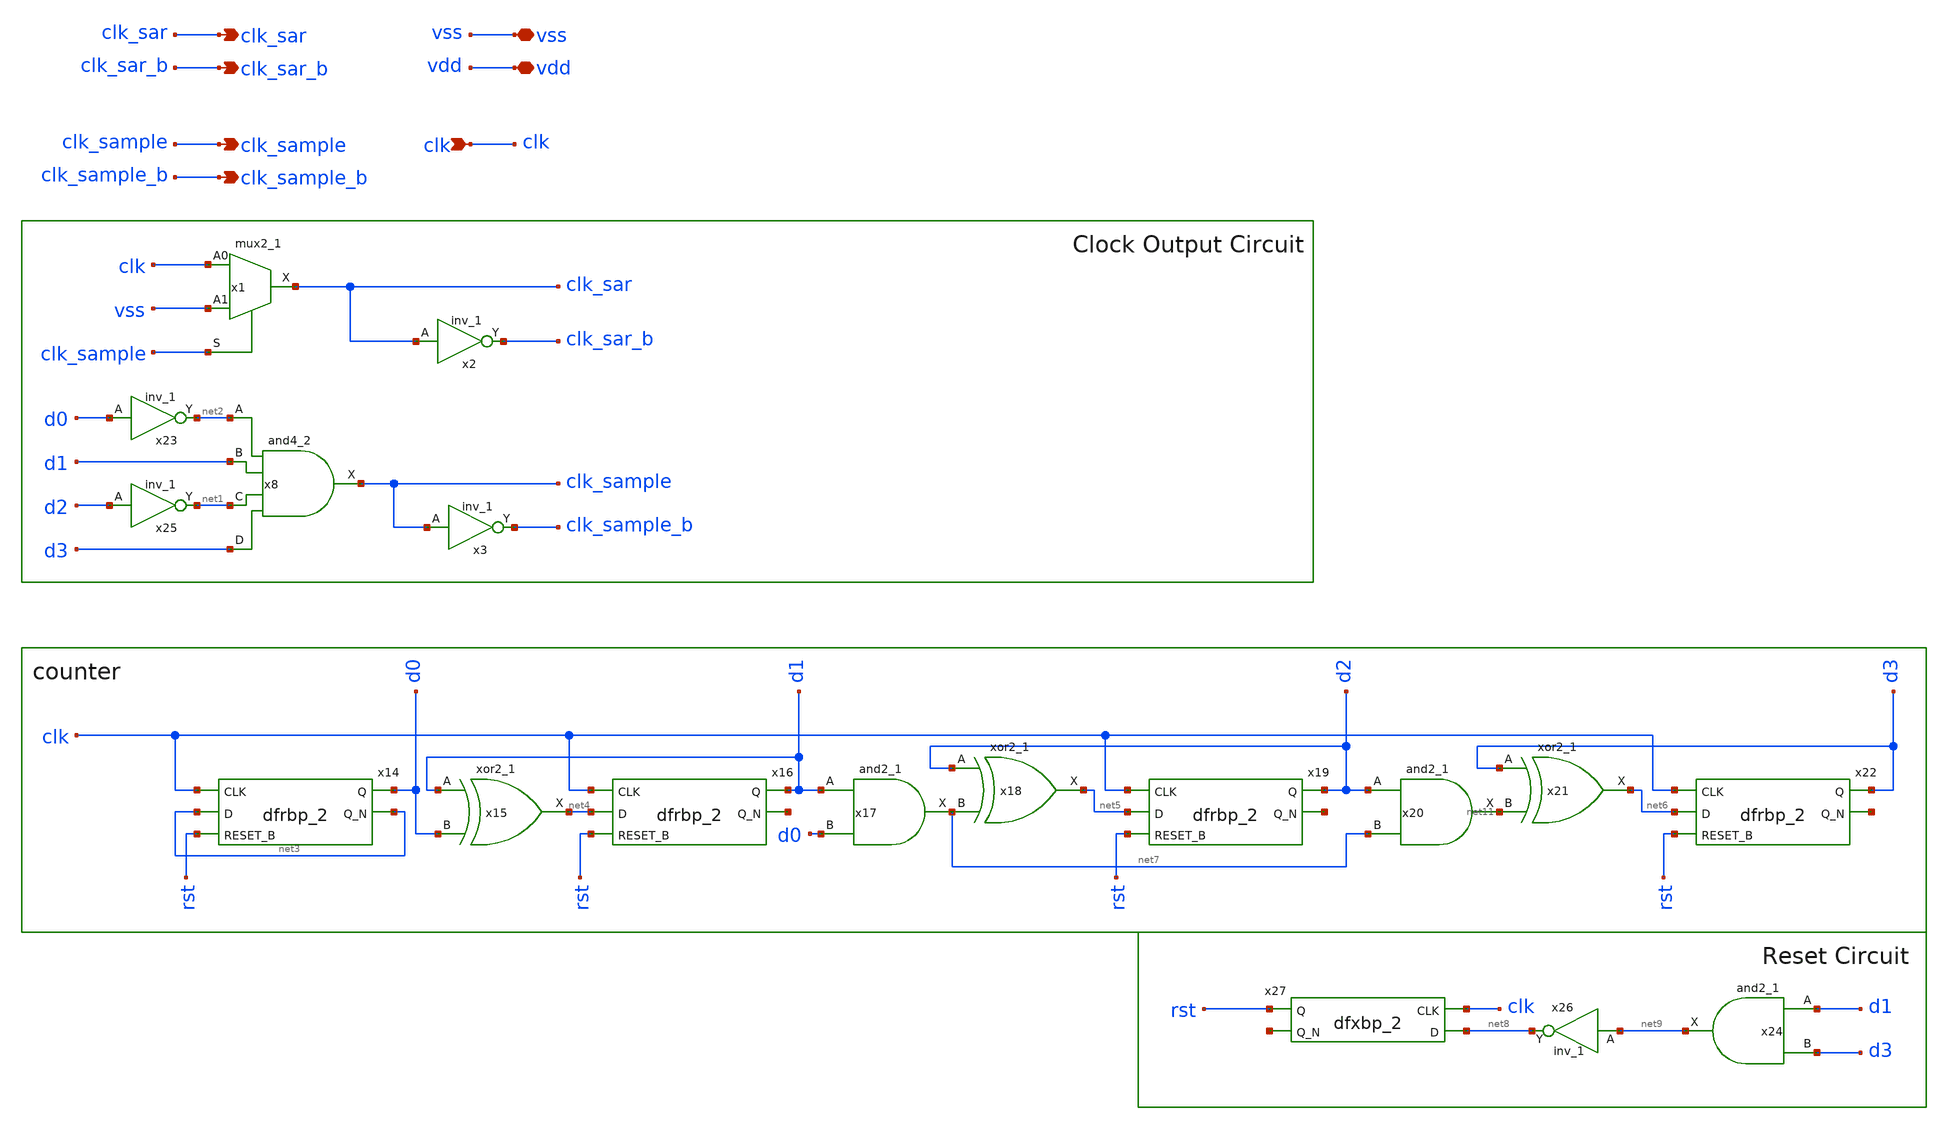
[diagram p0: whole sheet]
** sch_path: xschem/clockgen/clockgen.sch
**.subckt clockgen clk_sar clk_sample clk vss vdd clk_sar_b clk_sample_b
*.opin clk_sar
*.opin clk_sample
*.ipin clk
*.iopin vss
*.iopin vdd
*.opin clk_sar_b
*.opin clk_sample_b
x1 clk vss clk_sample vss vss vdd vdd clk_sar sky130_fd_sc_hd__mux2_1
x8 net2 d1 net1 d3 vss vss vdd vdd clk_sample sky130_fd_sc_hd__and4_2
x14 clk net3 rst vss vss vdd vdd d0 net3 sky130_fd_sc_hd__dfrbp_2
x15 d1 d0 vss vss vdd vdd net4 sky130_fd_sc_hd__xor2_1
x16 clk net4 rst vss vss vdd vdd d1 net10 sky130_fd_sc_hd__dfrbp_2
x17 d1 d0 vss vss vdd vdd net7 sky130_fd_sc_hd__and2_1
x18 d2 net7 vss vss vdd vdd net5 sky130_fd_sc_hd__xor2_1
x20 d2 net7 vss vss vdd vdd net11 sky130_fd_sc_hd__and2_1
x21 d3 net11 vss vss vdd vdd net6 sky130_fd_sc_hd__xor2_1
x19 clk net5 rst vss vss vdd vdd d2 net12 sky130_fd_sc_hd__dfrbp_2
x22 clk net6 rst vss vss vdd vdd d3 net13 sky130_fd_sc_hd__dfrbp_2
x23 d0 vss vss vdd vdd net2 sky130_fd_sc_hd__inv_1
x25 d2 vss vss vdd vdd net1 sky130_fd_sc_hd__inv_1
x24 d1 d3 vss vss vdd vdd net9 sky130_fd_sc_hd__and2_1
x26 net9 vss vss vdd vdd net8 sky130_fd_sc_hd__inv_1
x27 clk net8 vss vss vdd vdd rst net14 sky130_fd_sc_hd__dfxbp_2
x2 clk_sar vss vss vdd vdd clk_sar_b sky130_fd_sc_hd__inv_1
x3 clk_sample vss vss vdd vdd clk_sample_b sky130_fd_sc_hd__inv_1
**.ends
.end
